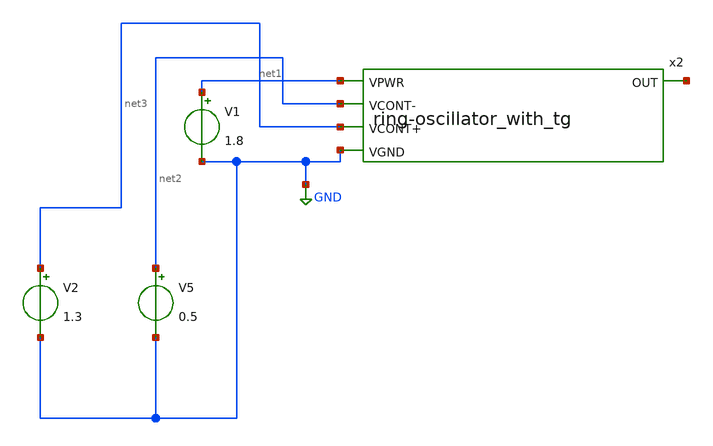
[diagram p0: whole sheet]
** sch_path: xschem_sch/ring-oscillator_with_tg_testbench.sch
**.subckt ring-oscillator_with_tg_testbench
V1 net1 GND 1.8
V2 net3 GND 1.3
x2 net1 net2 net4 net3 GND ring-oscillator_with_tg
V5 net2 GND 0.5
**** begin user architecture code


.option wnflag=1
.option savecurrents
.control
save all
tran 100n 1m 0
plot net4
op
.endc



** opencircuitdesign pdks install
.lib $::SKYWATER_MODELS/sky130.lib.spice tt
.param mc_mmm_cwitch=0
.param mc_pr_switch=1

**** end user architecture code
**.ends

* expanding   symbol:
*+  /home/raditya/Documents/Projects/Silicons/Projects/ring-oscillator_with_tg.sym # of pins=5
** sym_path: xschem_sch/ring-oscillator_with_tg.sym
** sch_path: xschem_sch/ring-oscillator_with_tg.sch
.subckt ring-oscillator_with_tg VPWR VCONT- OUT VCONT+ VGND
*.ipin VPWR
*.opin OUT
*.ipin VGND
*.ipin VCONT+
*.ipin VCONT-
XM7 net1 net5 VPWR VPWR sky130_fd_pr__pfet_01v8 L=0.2 W=0.45 nf=1 ad='int((nf+1)/2) * W/nf * 0.29' as='int((nf+2)/2) * W/nf * 0.29'
+ pd='2*int((nf+1)/2) * (W/nf + 0.29)' ps='2*int((nf+2)/2) * (W/nf + 0.29)' nrd='0.29 / W' nrs='0.29 / W'
+ sa=0 sb=0 sd=0 mult=1 m=1
XM8 net3 VCONT- net1 VPWR sky130_fd_pr__pfet_01v8 L=0.2 W=0.45 nf=1 ad='int((nf+1)/2) * W/nf * 0.29'
+ as='int((nf+2)/2) * W/nf * 0.29' pd='2*int((nf+1)/2) * (W/nf + 0.29)' ps='2*int((nf+2)/2) * (W/nf + 0.29)'
+ nrd='0.29 / W' nrs='0.29 / W' sa=0 sb=0 sd=0 mult=1 m=1
XM9 net2 net3 VPWR VPWR sky130_fd_pr__pfet_01v8 L=0.2 W=0.45 nf=1 ad='int((nf+1)/2) * W/nf * 0.29' as='int((nf+2)/2) * W/nf * 0.29'
+ pd='2*int((nf+1)/2) * (W/nf + 0.29)' ps='2*int((nf+2)/2) * (W/nf + 0.29)' nrd='0.29 / W' nrs='0.29 / W'
+ sa=0 sb=0 sd=0 mult=1 m=1
XM11 OUT net4 VPWR VPWR sky130_fd_pr__pfet_01v8 L=0.2 W=0.45 nf=1 ad='int((nf+1)/2) * W/nf * 0.29' as='int((nf+2)/2) * W/nf * 0.29'
+ pd='2*int((nf+1)/2) * (W/nf + 0.29)' ps='2*int((nf+2)/2) * (W/nf + 0.29)' nrd='0.29 / W' nrs='0.29 / W'
+ sa=0 sb=0 sd=0 mult=1 m=1
XM10 net4 VCONT- net2 VPWR sky130_fd_pr__pfet_01v8 L=0.2 W=0.45 nf=1 ad='int((nf+1)/2) * W/nf * 0.29'
+ as='int((nf+2)/2) * W/nf * 0.29' pd='2*int((nf+1)/2) * (W/nf + 0.29)' ps='2*int((nf+2)/2) * (W/nf + 0.29)'
+ nrd='0.29 / W' nrs='0.29 / W' sa=0 sb=0 sd=0 mult=1 m=1
XM12 net5 VCONT- OUT VPWR sky130_fd_pr__pfet_01v8 L=0.2 W=0.45 nf=1 ad='int((nf+1)/2) * W/nf * 0.29'
+ as='int((nf+2)/2) * W/nf * 0.29' pd='2*int((nf+1)/2) * (W/nf + 0.29)' ps='2*int((nf+2)/2) * (W/nf + 0.29)'
+ nrd='0.29 / W' nrs='0.29 / W' sa=0 sb=0 sd=0 mult=1 m=1
XC1 VGND net5 sky130_fd_pr__cap_mim_m3_1 W=10 L=10 MF=1 m=1
XC2 VGND net3 sky130_fd_pr__cap_mim_m3_1 W=10 L=10 MF=1 m=1
XC3 VGND net4 sky130_fd_pr__cap_mim_m3_1 W=10 L=10 MF=10 m=10
XM13 OUT net4 VGND VGND sky130_fd_pr__nfet_01v8 L=0.2 W=0.45 nf=1 ad='int((nf+1)/2) * W/nf * 0.29' as='int((nf+2)/2) * W/nf * 0.29'
+ pd='2*int((nf+1)/2) * (W/nf + 0.29)' ps='2*int((nf+2)/2) * (W/nf + 0.29)' nrd='0.29 / W' nrs='0.29 / W'
+ sa=0 sb=0 sd=0 mult=1 m=1
XM1 net2 net3 VGND VGND sky130_fd_pr__nfet_01v8 L=0.2 W=0.45 nf=1 ad='int((nf+1)/2) * W/nf * 0.29' as='int((nf+2)/2) * W/nf * 0.29'
+ pd='2*int((nf+1)/2) * (W/nf + 0.29)' ps='2*int((nf+2)/2) * (W/nf + 0.29)' nrd='0.29 / W' nrs='0.29 / W'
+ sa=0 sb=0 sd=0 mult=1 m=1
XM2 net1 net5 VGND VGND sky130_fd_pr__nfet_01v8 L=0.2 W=0.45 nf=1 ad='int((nf+1)/2) * W/nf * 0.29' as='int((nf+2)/2) * W/nf * 0.29'
+ pd='2*int((nf+1)/2) * (W/nf + 0.29)' ps='2*int((nf+2)/2) * (W/nf + 0.29)' nrd='0.29 / W' nrs='0.29 / W'
+ sa=0 sb=0 sd=0 mult=1 m=1
XM3 OUT VCONT+ net5 VGND sky130_fd_pr__nfet_01v8 L=0.2 W=0.45 nf=1 ad='int((nf+1)/2) * W/nf * 0.29' as='int((nf+2)/2) * W/nf * 0.29'
+ pd='2*int((nf+1)/2) * (W/nf + 0.29)' ps='2*int((nf+2)/2) * (W/nf + 0.29)' nrd='0.29 / W' nrs='0.29 / W'
+ sa=0 sb=0 sd=0 mult=1 m=1
XM4 net1 VCONT+ net3 VGND sky130_fd_pr__nfet_01v8 L=0.2 W=0.45 nf=1 ad='int((nf+1)/2) * W/nf * 0.29'
+ as='int((nf+2)/2) * W/nf * 0.29' pd='2*int((nf+1)/2) * (W/nf + 0.29)' ps='2*int((nf+2)/2) * (W/nf + 0.29)'
+ nrd='0.29 / W' nrs='0.29 / W' sa=0 sb=0 sd=0 mult=1 m=1
XM5 net2 VCONT+ net4 VGND sky130_fd_pr__nfet_01v8 L=0.2 W=0.45 nf=1 ad='int((nf+1)/2) * W/nf * 0.29'
+ as='int((nf+2)/2) * W/nf * 0.29' pd='2*int((nf+1)/2) * (W/nf + 0.29)' ps='2*int((nf+2)/2) * (W/nf + 0.29)'
+ nrd='0.29 / W' nrs='0.29 / W' sa=0 sb=0 sd=0 mult=1 m=1
.ends

.GLOBAL GND
.end
